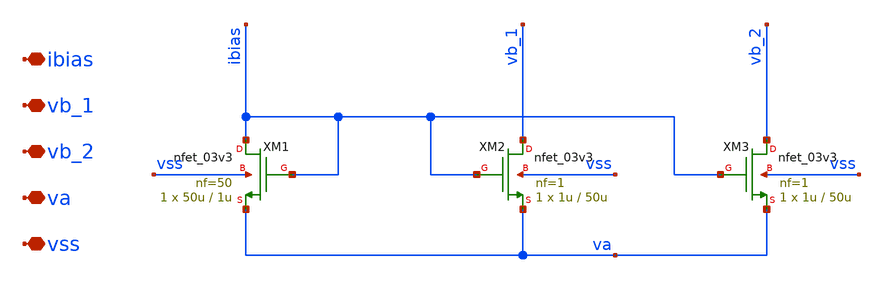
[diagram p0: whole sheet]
** sch_path: xschem/archive/pseudores/pseudores.sch
**.subckt pseudores ibias vb_1 vb_2 va vss
*.iopin ibias
*.iopin vb_1
*.iopin vb_2
*.iopin va
*.iopin vss
XM1 ibias ibias va vss nfet_03v3 L=1u W=50u nf=50 ad='int((nf+1)/2) * W/nf * 0.18u' as='int((nf+2)/2) * W/nf * 0.18u'
+ pd='2*int((nf+1)/2) * (W/nf + 0.18u)' ps='2*int((nf+2)/2) * (W/nf + 0.18u)' nrd='0.18u / W' nrs='0.18u / W'
+ sa=0 sb=0 sd=0 m=1
XM2 vb_1 ibias va vss nfet_03v3 L=50u W=1u nf=1 ad='int((nf+1)/2) * W/nf * 0.18u' as='int((nf+2)/2) * W/nf * 0.18u'
+ pd='2*int((nf+1)/2) * (W/nf + 0.18u)' ps='2*int((nf+2)/2) * (W/nf + 0.18u)' nrd='0.18u / W' nrs='0.18u / W'
+ sa=0 sb=0 sd=0 m=1
XM3 vb_2 ibias va vss nfet_03v3 L=50u W=1u nf=1 ad='int((nf+1)/2) * W/nf * 0.18u' as='int((nf+2)/2) * W/nf * 0.18u'
+ pd='2*int((nf+1)/2) * (W/nf + 0.18u)' ps='2*int((nf+2)/2) * (W/nf + 0.18u)' nrd='0.18u / W' nrs='0.18u / W'
+ sa=0 sb=0 sd=0 m=1
**.ends
.end
